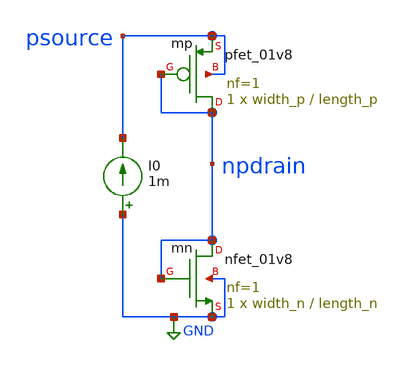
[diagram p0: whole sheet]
** sch_path: ISSCC25/submitted_notebooks/current_mirror_ota_optimization/characterization/sky130/characterization_script_sandbox_rundir/cid_characterization.sch
**.subckt cid_characterization
xmp npdrain npdrain psource psource sky130_fd_pr__pfet_01v8 L=length_p W=width_p nf=1 ad='int((nf+1)/2) * W/nf * 0.29'
+ as='int((nf+2)/2) * W/nf * 0.29' pd='2*int((nf+1)/2) * (W/nf + 0.29)' ps='2*int((nf+2)/2) * (W/nf + 0.29)'
+ nrd='0.29 / W' nrs='0.29 / W' sa=0 sb=0 sd=0 mult=1 m=1
I0 GND psource 1m
xmn npdrain npdrain GND GND sky130_fd_pr__nfet_01v8 L=length_n W=width_n nf=1 ad='int((nf+1)/2) * W/nf * 0.29'
+ as='int((nf+2)/2) * W/nf * 0.29' pd='2*int((nf+1)/2) * (W/nf + 0.29)' ps='2*int((nf+2)/2) * (W/nf + 0.29)'
+ nrd='0.29 / W' nrs='0.29 / W' sa=0 sb=0 sd=0 mult=1 m=1
**** begin user architecture code



* geometry parameters
.param width_p = 1
.param width_n = 1
.param length_p = 0.15
.param length_n = 0.15
.param l = 0.15
.param w = 1

* sweep parameters
* .param start = 1u
* .param stop = 1m
* .param points_per_decade 25

.temp 27

.lib /opt/pdk/open_pdks/sky130/sky130A/libs.tech/ngspice/sky130.lib.spice tt
.control

let start = 1n
let stop = 1m
let points_per_decade = 20

let stop_start_ratio = stop/start
let num_decades = log10(stop_start_ratio)

echo Stop/Start Ratio $&stop_start_ratio
echo Characterizing $&num_decades decades from $&start to $&stop
echo Simulating $&points_per_decade points per decade
echo

let i_start = start
let i_end = i_start*10
let i_step = i_end/points_per_decade
let i_end = i_end - i_step


* let length_n_counter = length_n
* let length_p_counter = length_p

set pl = 0.15
set nl = 0.15

* Iterate for 10 different transistor lengths
set lengths = 10
let i = 0
let length_increment = 0.15
set appendwrite

echo ' isweep  gm  i_id  id  i_cgg  cgg  i_cgs  cgs  i_cgd  cgd  i_cds  cds  i_css  css  i_cdd  cdd  i_gds  gds  i_vth  vth  i_vdsat  vdsat  i_vgs  vgs  i_vds  vds  i_rds  rds  i_wt  wt  i_ft  ft  i_gm_id  gm_id'
+ > nfet_cid_characterization.csv
echo ' isweep  gm  i_id  id  i_cgg  cgg  i_cgs  cgs  i_cgd  cgd  i_cds  cds  i_css  css  i_cdd  cdd  i_gds  gds  i_vth  vth  i_vdsat  vdsat  i_vgs  vgs  i_vds  vds  i_rds  rds  i_wt  wt  i_ft  ft  i_gm_id  gm_id'
+ > pfet_cid_characterization.csv


while i < num_decades

	set filetype=ascii
	set hcopydevtype=svg
	set format = cross
	save @m.xmn.msky130_fd_pr__nfet_01v8[gm]
	save @m.xmn.msky130_fd_pr__nfet_01v8[id]
	save @m.xmn.msky130_fd_pr__nfet_01v8[cgg]
	save @m.xmn.msky130_fd_pr__nfet_01v8[cgs]
	save @m.xmn.msky130_fd_pr__nfet_01v8[cgd]
	save @m.xmn.msky130_fd_pr__nfet_01v8[cds]
	save @m.xmn.msky130_fd_pr__nfet_01v8[css]
	save @m.xmn.msky130_fd_pr__nfet_01v8[cdd]
	save @m.xmn.msky130_fd_pr__nfet_01v8[gds]
	save @m.xmn.msky130_fd_pr__nfet_01v8[vth]
	save @m.xmn.msky130_fd_pr__nfet_01v8[vdsat]
	save @m.xmn.msky130_fd_pr__nfet_01v8[vgs]
	save @m.xmn.msky130_fd_pr__nfet_01v8[vds]

	save @m.xmp.msky130_fd_pr__pfet_01v8[gm]
	save @m.xmp.msky130_fd_pr__pfet_01v8[id]
	save @m.xmp.msky130_fd_pr__pfet_01v8[cgg]
	save @m.xmp.msky130_fd_pr__pfet_01v8[cgs]
	save @m.xmp.msky130_fd_pr__pfet_01v8[cgd]
	save @m.xmp.msky130_fd_pr__pfet_01v8[cds]
	save @m.xmp.msky130_fd_pr__pfet_01v8[css]
	save @m.xmp.msky130_fd_pr__pfet_01v8[cdd]
	save @m.xmp.msky130_fd_pr__pfet_01v8[gds]
	save @m.xmp.msky130_fd_pr__pfet_01v8[vth]
	save @m.xmp.msky130_fd_pr__pfet_01v8[vdsat]
	save @m.xmp.msky130_fd_pr__pfet_01v8[vgs]
	save @m.xmp.msky130_fd_pr__pfet_01v8[vds]

	let step_size = (stop/start)
	echo Simulating rom $&i_start to $&i_end with step size of $&i_step
	dc I0 $&i_start $&i_end $&i_step

	* Note let is for vectors and set is for scalars

	let n_gm = @m.xmn.msky130_fd_pr__nfet_01v8[gm]
	let n_id = @m.xmn.msky130_fd_pr__nfet_01v8[id]
	let n_cgg = @m.xmn.msky130_fd_pr__nfet_01v8[cgg]
	let n_cgs = @m.xmn.msky130_fd_pr__nfet_01v8[cgs]
	let n_cgd = @m.xmn.msky130_fd_pr__nfet_01v8[cgd]
	let n_cds = @m.xmn.msky130_fd_pr__nfet_01v8[cds]
	let n_css = @m.xmn.msky130_fd_pr__nfet_01v8[css]
	let n_cdd = @m.xmn.msky130_fd_pr__nfet_01v8[cdd]
	let n_gds = @m.xmn.msky130_fd_pr__nfet_01v8[gds]
	let n_vth = @m.xmn.msky130_fd_pr__nfet_01v8[vth]
	let n_vdsat = @m.xmn.msky130_fd_pr__nfet_01v8[vdsat]
	let n_vgs = @m.xmn.msky130_fd_pr__nfet_01v8[vgs]
	let n_vds = @m.xmn.msky130_fd_pr__nfet_01v8[vds]

	let p_gm = @m.xmp.msky130_fd_pr__pfet_01v8[gm]
	let p_id = @m.xmp.msky130_fd_pr__pfet_01v8[id]
	let p_cgg = @m.xmp.msky130_fd_pr__pfet_01v8[cgg]
	let p_cgs = @m.xmp.msky130_fd_pr__pfet_01v8[cgs]
	let p_cgd = @m.xmp.msky130_fd_pr__pfet_01v8[cgd]
	let p_cds = @m.xmp.msky130_fd_pr__pfet_01v8[cds]
	let p_css = @m.xmp.msky130_fd_pr__pfet_01v8[css]
	let p_cdd = @m.xmp.msky130_fd_pr__pfet_01v8[cdd]
	let p_gds = @m.xmp.msky130_fd_pr__pfet_01v8[gds]
	let p_vth = @m.xmp.msky130_fd_pr__pfet_01v8[vth]
	let p_vdsat = @m.xmp.msky130_fd_pr__pfet_01v8[vdsat]
	let p_vgs = @m.xmp.msky130_fd_pr__pfet_01v8[vgs]
	let p_vds = @m.xmp.msky130_fd_pr__pfet_01v8[vds]

	let n_rds = 1/n_gds
	let n_wt = n_gm/n_cgg
	let n_ft = n_wt/(2*pi)
	let n_gm_id = n_gm/n_id

	let p_rds = 1/p_gds
	let p_wt = p_gm/p_cgg
	let p_ft = p_wt/(2*pi)
	let p_gm_id = p_gm/p_id


	* write writes the outputs with information - use wrdata instead
	* write nfet_cid_characterization.txt n_gm n_id n_cgg n_cgs n_cgd n_cds n_css n_cdd n_gds n_vth
+ n_vdsat n_vgs n_vds n_rds n_wt n_ft n_gm_id
	* write pfet_cid_characterization.txt p_gm p_id p_cgg p_cgs p_cgd p_cds p_css p_cdd p_gds p_vth
+ p_vdsat p_vgs p_vds p_rds p_wt p_ft p_gm_id

	wrdata nfet_cid_characterization.csv n_gm n_id n_cgg n_cgs n_cgd n_cds n_css n_cdd n_gds n_vth
+ n_vdsat n_vgs n_vds n_rds n_wt n_ft n_gm_id
	wrdata pfet_cid_characterization.csv p_gm p_id p_cgg p_cgs p_cgd p_cds p_css p_cdd p_gds p_vth
+ p_vdsat p_vgs p_vds p_rds p_wt p_ft p_gm_id

	* print n_gm n_id n_cgg n_cgs n_cgd n_cds n_css n_cdd n_gds n_vth n_vdsat n_vgs n_vds n_rds n_wt
+ n_ft n_gm_id >> nfet_cid_characterization.csv
	* alterparam length_p = pl
	* alterparam length_n = nl
	let i_start = i_start*10
	let i_end = i_start*10
	let i_step = i_end/points_per_decade
	let i_end = i_end - i_step
	let i = i + 1
end

* plot ft_n vs gm_id_n ylog


.endc


.save all



**** end user architecture code
**.ends
.GLOBAL GND
.end
